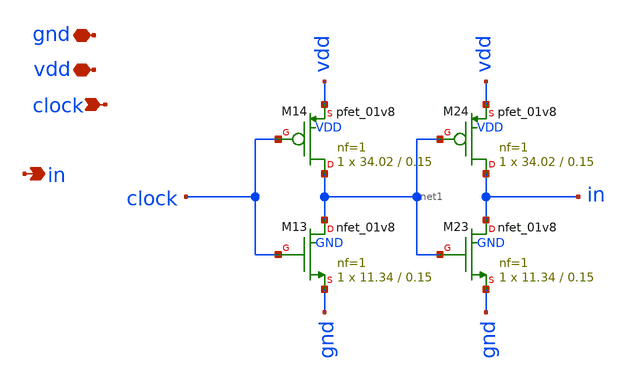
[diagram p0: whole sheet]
** sch_path: xschem/charge_pumps2/buffer.sch
**.subckt buffer clock vdd gnd in
*.ipin clock
*.iopin vdd
*.iopin gnd
*.opin in
XM13 net1 clock gnd GND sky130_fd_pr__nfet_01v8 L=0.15 W=11.34 nf=1 ad='int((nf+1)/2) * W/nf * 0.29'
+ as='int((nf+2)/2) * W/nf * 0.29' pd='2*int((nf+1)/2) * (W/nf + 0.29)' ps='2*int((nf+2)/2) * (W/nf + 0.29)'
+ nrd='0.29 / W' nrs='0.29 / W' sa=0 sb=0 sd=0 mult=1 m=1
XM14 net1 clock vdd VDD sky130_fd_pr__pfet_01v8 L=0.15 W=34.02 nf=1 ad='int((nf+1)/2) * W/nf * 0.29'
+ as='int((nf+2)/2) * W/nf * 0.29' pd='2*int((nf+1)/2) * (W/nf + 0.29)' ps='2*int((nf+2)/2) * (W/nf + 0.29)'
+ nrd='0.29 / W' nrs='0.29 / W' sa=0 sb=0 sd=0 mult=1 m=1
XM23 in net1 gnd GND sky130_fd_pr__nfet_01v8 L=0.15 W=11.34 nf=1 ad='int((nf+1)/2) * W/nf * 0.29' as='int((nf+2)/2) * W/nf * 0.29'
+ pd='2*int((nf+1)/2) * (W/nf + 0.29)' ps='2*int((nf+2)/2) * (W/nf + 0.29)' nrd='0.29 / W' nrs='0.29 / W'
+ sa=0 sb=0 sd=0 mult=1 m=1
XM24 in net1 vdd VDD sky130_fd_pr__pfet_01v8 L=0.15 W=34.02 nf=1 ad='int((nf+1)/2) * W/nf * 0.29' as='int((nf+2)/2) * W/nf * 0.29'
+ pd='2*int((nf+1)/2) * (W/nf + 0.29)' ps='2*int((nf+2)/2) * (W/nf + 0.29)' nrd='0.29 / W' nrs='0.29 / W'
+ sa=0 sb=0 sd=0 mult=1 m=1
**.ends
.end
